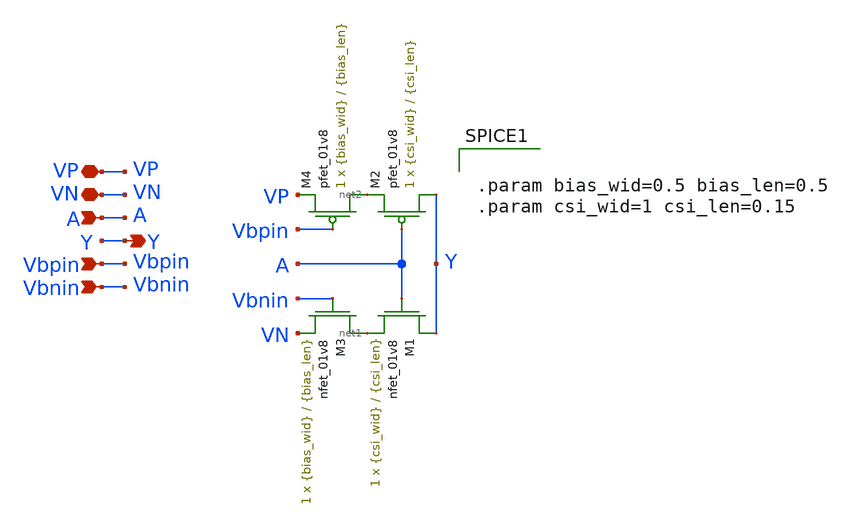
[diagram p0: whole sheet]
** sch_path: LDS/LDS_csi.sch
**.subckt LDS_csi VN VP Y Vbpin A Vbnin
*.iopin VN
*.iopin VP
*.opin Y
*.ipin Vbpin
*.ipin A
*.ipin Vbnin
XM1 Y A net1 VN sky130_fd_pr__nfet_01v8 L={csi_len} W={csi_wid} nf=1 ad='int((nf+1)/2) * W/nf * 0.29'
+ as='int((nf+2)/2) * W/nf * 0.29' pd='2*int((nf+1)/2) * (W/nf + 0.29)' ps='2*int((nf+2)/2) * (W/nf + 0.29)'
+ nrd='0.29 / W' nrs='0.29 / W' sa=0 sb=0 sd=0 mult=1 m=1
XM2 Y A net2 VP sky130_fd_pr__pfet_01v8 L={csi_len} W={csi_wid} nf=1 ad='int((nf+1)/2) * W/nf * 0.29'
+ as='int((nf+2)/2) * W/nf * 0.29' pd='2*int((nf+1)/2) * (W/nf + 0.29)' ps='2*int((nf+2)/2) * (W/nf + 0.29)'
+ nrd='0.29 / W' nrs='0.29 / W' sa=0 sb=0 sd=0 mult=1 m=1
XM3 net1 Vbnin VN VN sky130_fd_pr__nfet_01v8 L={bias_len} W={bias_wid} nf=1 ad='int((nf+1)/2) * W/nf * 0.29'
+ as='int((nf+2)/2) * W/nf * 0.29' pd='2*int((nf+1)/2) * (W/nf + 0.29)' ps='2*int((nf+2)/2) * (W/nf + 0.29)'
+ nrd='0.29 / W' nrs='0.29 / W' sa=0 sb=0 sd=0 mult=1 m=1
XM4 net2 Vbpin VP VP sky130_fd_pr__pfet_01v8 L={bias_len} W={bias_wid} nf=1 ad='int((nf+1)/2) * W/nf * 0.29'
+ as='int((nf+2)/2) * W/nf * 0.29' pd='2*int((nf+1)/2) * (W/nf + 0.29)' ps='2*int((nf+2)/2) * (W/nf + 0.29)'
+ nrd='0.29 / W' nrs='0.29 / W' sa=0 sb=0 sd=0 mult=1 m=1
**** begin user architecture code


.param bias_wid=0.5 bias_len=0.5
.param csi_wid=1 csi_len=0.15


**** end user architecture code
**.ends
.end
